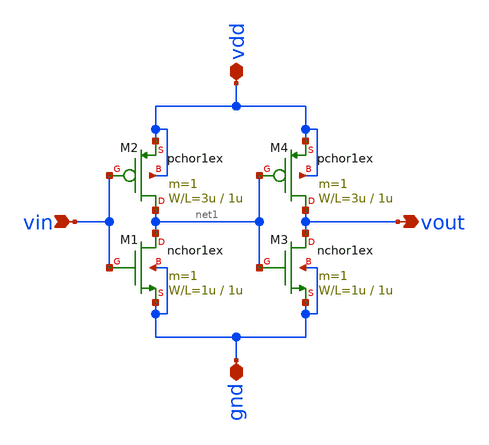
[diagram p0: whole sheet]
** sch_path: member_project/DCDC_DOWN/xschem/original_VCO/buffer.sch
**.subckt buffer vdd vin vout gnd
*.iopin vdd
*.ipin vin
*.opin vout
*.iopin gnd
M1 net1 vin gnd gnd nchor1ex L=1u W=1u m=1
M2 net1 vin vdd vdd pchor1ex L=1u W=3u m=1
M3 vout net1 gnd gnd nchor1ex L=1u W=1u m=1
M4 vout net1 vdd vdd pchor1ex L=1u W=3u m=1
**.ends
.end
